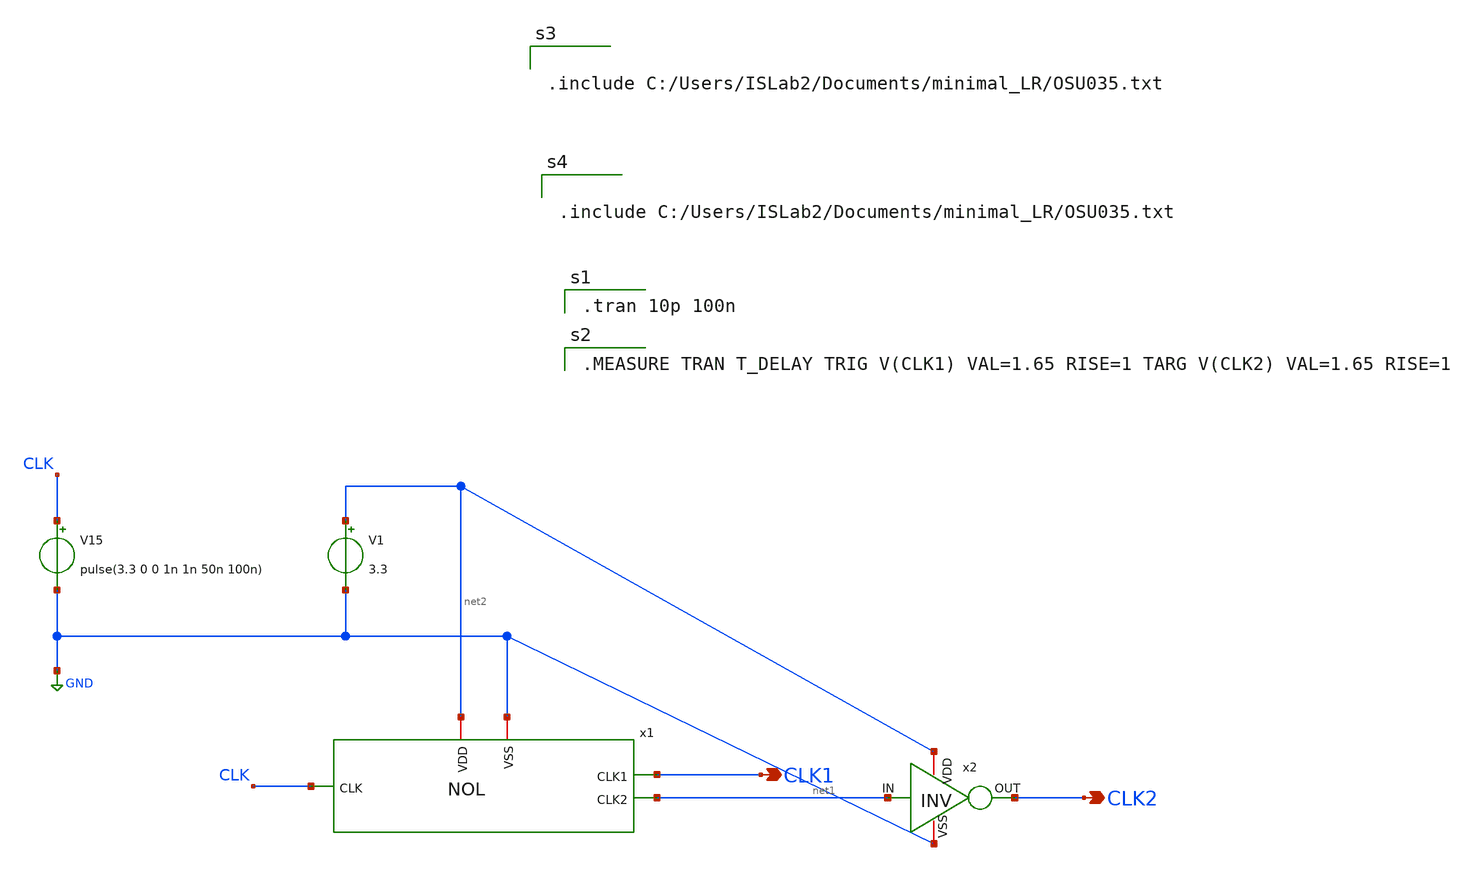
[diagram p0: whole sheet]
** sch_path: NOL_sim.sch
**.subckt NOL_sim CLK1 CLK2
*.opin CLK1
*.opin CLK2
x1 net2 CLK CLK1 GND net1 NOL
V15 CLK GND pulse(3.3 0 0 1n 1n 50n 100n)
V1 net2 GND 3.3
x2 net2 CLK2 net1 GND INV
**** begin user architecture code

.tran 10p 100n


.MEASURE TRAN T_DELAY TRIG V(CLK1) VAL=1.65 RISE=1 TARG V(CLK2) VAL=1.65 RISE=1



.include C:/Users/ISLab2/Documents/minimal_LR/OSU035.txt



.include C:/Users/ISLab2/Documents/minimal_LR/OSU035.txt

**** end user architecture code
**.ends

* expanding   symbol:  NOL.sym # of pins=5
** sym_path: NOL.sym
** sch_path: NOL.sch
.subckt NOL VDD CLK CLK1 VSS CLK2
*.ipin CLK
*.opin CLK1
*.opin CLK2
*.iopin VDD
*.iopin VSS
x3 VDD net1 CLK VSS INV
x1 VDD CLK net9 CLK2 VSS NOR
x2 VDD CLK1 net2 net1 VSS NOR
x4 VDD net3 net2 VSS INV
x5 VDD net4 net3 VSS INV
x6 VDD net5 net4 VSS INV
x7 VDD net17 net5 VSS INV
x8 VDD net6 net9 VSS INV
x9 VDD net7 net6 VSS INV
x10 VDD net8 net7 VSS INV
x11 VDD net13 net8 VSS INV
x12 VDD net10 net13 VSS INV
x13 VDD net11 net10 VSS INV
x14 VDD net12 net11 VSS INV
x15 VDD net32 net12 VSS INV
x16 VDD net14 net17 VSS INV
x17 VDD net15 net14 VSS INV
x18 VDD net16 net15 VSS INV
x19 VDD net33 net16 VSS INV
x20 VDD net18 net33 VSS INV
x21 VDD net19 net18 VSS INV
x22 VDD net20 net19 VSS INV
x23 VDD net24 net20 VSS INV
x24 VDD net21 net24 VSS INV
x25 VDD net22 net21 VSS INV
x26 VDD net23 net22 VSS INV
x27 VDD net34 net23 VSS INV
x28 VDD net25 net32 VSS INV
x29 VDD net26 net25 VSS INV
x30 VDD net27 net26 VSS INV
x31 VDD net31 net27 VSS INV
x32 VDD net28 net31 VSS INV
x33 VDD net29 net28 VSS INV
x34 VDD net30 net29 VSS INV
x35 VDD net50 net30 VSS INV
x36 VDD net35 net34 VSS INV
x37 VDD net36 net35 VSS INV
x38 VDD net37 net36 VSS INV
x39 VDD net41 net37 VSS INV
x40 VDD net38 net41 VSS INV
x41 VDD net39 net38 VSS INV
x42 VDD net40 net39 VSS INV
x43 VDD net42 net40 VSS INV
x44 VDD net43 net50 VSS INV
x45 VDD net44 net43 VSS INV
x46 VDD net45 net44 VSS INV
x47 VDD net49 net45 VSS INV
x48 VDD net46 net49 VSS INV
x49 VDD net47 net46 VSS INV
x50 VDD net48 net47 VSS INV
x51 VDD net61 net48 VSS INV
x52 VDD net51 net42 VSS INV
x53 VDD net53 net51 VSS INV
x54 VDD net52 net61 VSS INV
x55 VDD net60 net52 VSS INV
x56 VDD net54 net53 VSS INV
x57 VDD net55 net54 VSS INV
x58 VDD net56 net55 VSS INV
x59 VDD CLK2 net56 VSS INV
x64 VDD net57 net60 VSS INV
x65 VDD net58 net57 VSS INV
x66 VDD net59 net58 VSS INV
x67 VDD CLK1 net59 VSS INV
.ends


* expanding   symbol:  INV.sym # of pins=4
** sym_path: INV.sym
** sch_path: INV.sch
.subckt INV VDD OUT IN VSS
*.opin OUT
*.ipin IN
*.iopin VDD
*.iopin VSS
M2 OUT IN VDD VDD pch w=5u l=0.35u as=0 ps=0 ad=0 pd=0 m=1
M1 OUT IN VSS VSS nch w=2.5u l=0.35u as=0 ps=0 ad=0 pd=0 m=1
.ends


* expanding   symbol:  NOR.sym # of pins=5
** sym_path: NOR.sym
** sch_path: NOR.sch
.subckt NOR VDD A Y B VSS
*.iopin VDD
*.ipin A
*.ipin B
*.iopin VSS
*.opin Y
M1 Y A VSS VSS nch w=3.5u l=0.35u as=0 ps=0 ad=0 pd=0 m=1
M2 net1 A VDD VDD pch w=3.5u l=0.35u as=0 ps=0 ad=0 pd=0 m=1
M3 Y B net1 VDD pch w=3.5u l=0.35u as=0 ps=0 ad=0 pd=0 m=1
M4 Y B VSS VSS nch w=3.5u l=0.35u as=0 ps=0 ad=0 pd=0 m=1
.ends

.GLOBAL GND
.end
